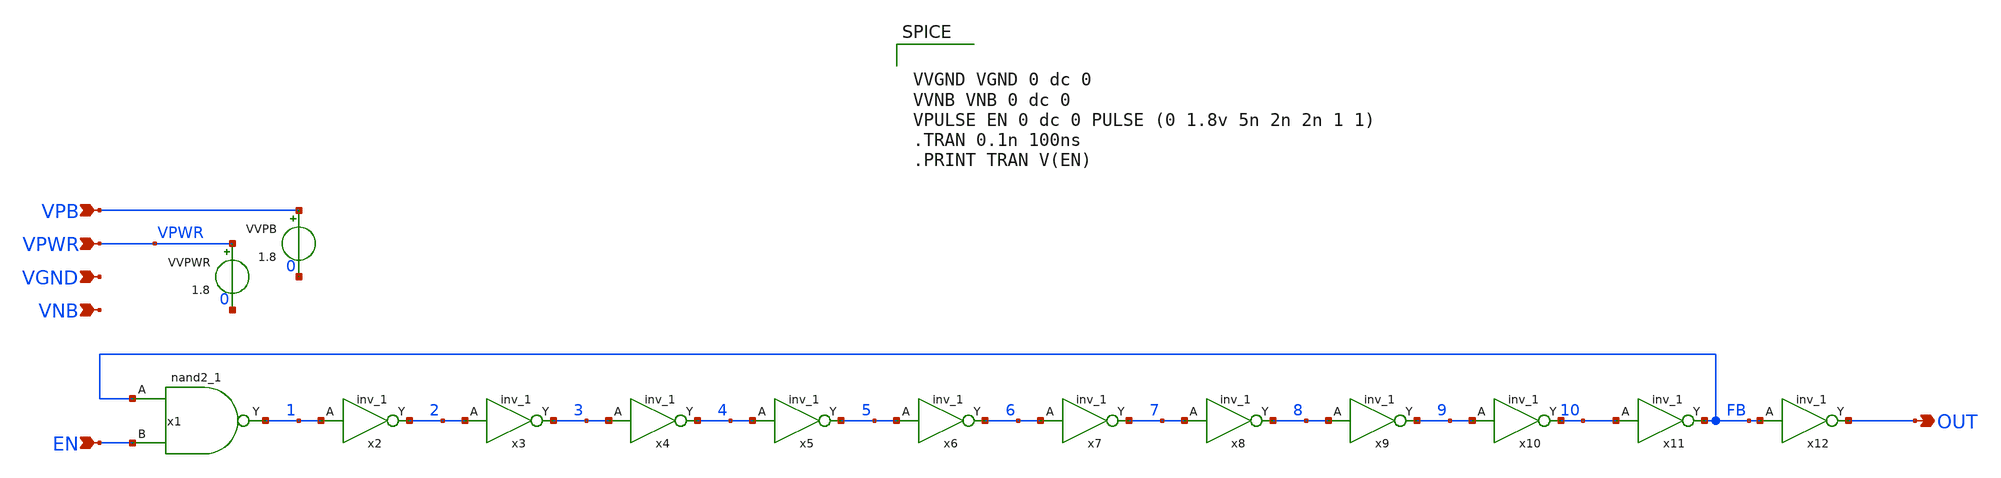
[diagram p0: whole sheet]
** sch_path: skywater/ringo.sch


VVGND VGND 0 dc 0
VVNB VNB 0 dc 0
VPULSE EN 0 dc 0 PULSE (0 1.8v 5n 2n 2n 1 1)
.TRAN 0.1n 100ns
.PRINT TRAN V(EN)



.lib $::SKYWATER_MODELS/models/sky130.lib.spice tt
.include $::SKYWATER_STDCELLS/cells/inv/sky130_fd_sc_hd__inv_1.spice
.include $::SKYWATER_STDCELLS/cells/nand2/sky130_fd_sc_hd__nand2_1.spice

**.subckt ringo EN OUT VPB VPWR VGND VNB
*.ipin EN
*.opin OUT
*.ipin VPB
*.ipin VPWR
*.ipin VGND
*.ipin VNB
x1 FB EN VGND VNB VPB VPWR 1 sky130_fd_sc_hd__nand2_1
x2 1 VGND VNB VPB VPWR 2 sky130_fd_sc_hd__inv_1
x3 2 VGND VNB VPB VPWR 3 sky130_fd_sc_hd__inv_1
x4 3 VGND VNB VPB VPWR 4 sky130_fd_sc_hd__inv_1
x5 4 VGND VNB VPB VPWR 5 sky130_fd_sc_hd__inv_1
x6 5 VGND VNB VPB VPWR 6 sky130_fd_sc_hd__inv_1
x7 6 VGND VNB VPB VPWR 7 sky130_fd_sc_hd__inv_1
x8 7 VGND VNB VPB VPWR 8 sky130_fd_sc_hd__inv_1
x9 8 VGND VNB VPB VPWR 9 sky130_fd_sc_hd__inv_1
x10 9 VGND VNB VPB VPWR 10 sky130_fd_sc_hd__inv_1
x11 10 VGND VNB VPB VPWR FB sky130_fd_sc_hd__inv_1
x12 FB VGND VNB VPB VPWR OUT sky130_fd_sc_hd__inv_1
VVPB VPB 0 1.8
VVPWR VPWR 0 1.8
**.ends
.end
